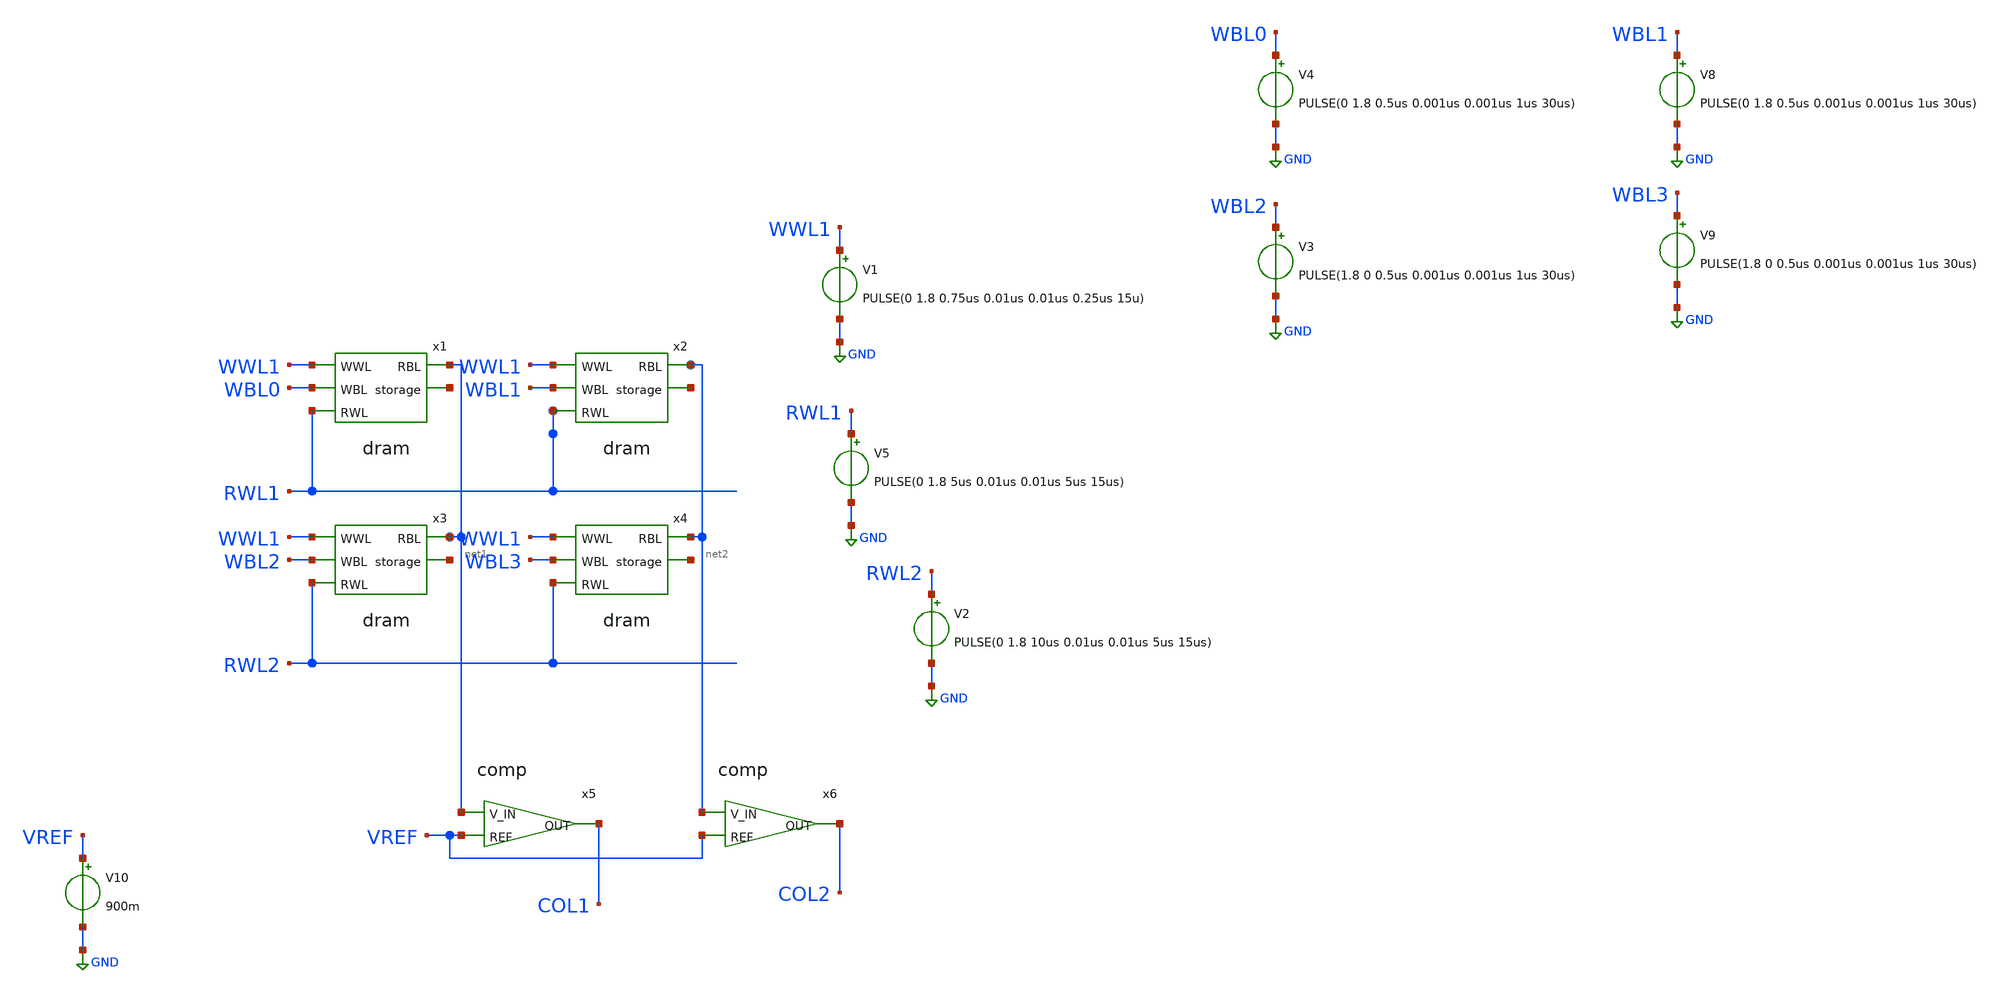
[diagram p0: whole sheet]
** sch_path: xschem/digital_prims/dram_tb.sch
**.subckt dram_tb
V1 WWL1 GND PULSE(0 1.8 0.75us 0.01us 0.01us 0.25us 15u)
V4 WBL0 GND PULSE(0 1.8 0.5us 0.001us 0.001us 1us 30us)
V5 RWL1 GND PULSE(0 1.8 5us 0.01us 0.01us 5us 15us)
x1 WWL1 net1 net3 WBL0 RWL1 dram
x2 WWL1 net2 net4 WBL1 RWL1 dram
x3 WWL1 net1 net5 WBL2 RWL2 dram
x4 WWL1 net2 net6 WBL3 RWL2 dram
V2 RWL2 GND PULSE(0 1.8 10us 0.01us 0.01us 5us 15us)
V3 WBL2 GND PULSE(1.8 0 0.5us 0.001us 0.001us 1us 30us)
V8 WBL1 GND PULSE(0 1.8 0.5us 0.001us 0.001us 1us 30us)
V9 WBL3 GND PULSE(1.8 0 0.5us 0.001us 0.001us 1us 30us)
x5 COL1 net1 VREF comp
x6 COL2 net2 VREF comp
V10 VREF GND 900m
**** begin user architecture code

** opencircuitdesign pdks install
.lib $::SKYWATER_MODELS/sky130.lib.spice tt


**** end user architecture code
**.ends

* expanding   symbol:  dram.sym # of pins=5
** sym_path: xschem/digital_prims/dram.sym
** sch_path: xschem/digital_prims/dram.sch
.subckt dram WWL RBL storage WBL RWL
*.opin RBL
*.ipin RWL
*.ipin WBL
*.ipin WWL
*.opin storage
XM3 RWL storage RBL GND sky130_fd_pr__nfet_01v8 L=0.15 W=1 nf=1 ad='int((nf+1)/2) * W/nf * 0.29' as='int((nf+2)/2) * W/nf * 0.29'
+ pd='2*int((nf+1)/2) * (W/nf + 0.29)' ps='2*int((nf+2)/2) * (W/nf + 0.29)' nrd='0.29 / W' nrs='0.29 / W'
+ sa=0 sb=0 sd=0 mult=1 m=1
XM1 WBL WWL storage GND sky130_fd_pr__nfet_01v8 L=0.15 W=1 nf=1 ad='int((nf+1)/2) * W/nf * 0.29' as='int((nf+2)/2) * W/nf * 0.29'
+ pd='2*int((nf+1)/2) * (W/nf + 0.29)' ps='2*int((nf+2)/2) * (W/nf + 0.29)' nrd='0.29 / W' nrs='0.29 / W'
+ sa=0 sb=0 sd=0 mult=1 m=1
.ends


* expanding   symbol:  comp.sym # of pins=3
** sym_path: xschem/comp.sym
** sch_path: xschem/comp.sch
.subckt comp OUT V_IN REF
*.ipin REF
*.ipin V_IN
*.opin OUT
XM5 net1 GN VCC VCC sky130_fd_pr__pfet_01v8_lvt L=1 W=1 nf=1 ad='W * 0.29' as='W * 0.29' pd='2*(W + 0.29)'
+ ps='2*(W + 0.29)' nrd=0 nrs=0 sa=0 sb=0 sd=0 mult=1 m=1
XM6 GN GN VCC VCC sky130_fd_pr__pfet_01v8_lvt L=1 W=1 nf=1 ad='W * 0.29' as='W * 0.29' pd='2*(W + 0.29)'
+ ps='2*(W + 0.29)' nrd=0 nrs=0 sa=0 sb=0 sd=0 mult=1 m=1
XM23 net1 V_IN SN GND sky130_fd_pr__nfet_01v8_lvt L=0.15 W=1 nf=1 ad='W * 0.29' as='W * 0.29' pd='2*(W + 0.29)'
+ ps='2*(W + 0.29)' nrd=0 nrs=0 sa=0 sb=0 sd=0 mult=1 m=1
XM16 GN REF SN GND sky130_fd_pr__nfet_01v8_lvt L=0.15 W=1 nf=1 ad='W * 0.29' as='W * 0.29' pd='2*(W + 0.29)'
+ ps='2*(W + 0.29)' nrd=0 nrs=0 sa=0 sb=0 sd=0 mult=1 m=1
I0 SN GND 100n
XM1 OUT net1 GND GND sky130_fd_pr__nfet_01v8_lvt L=0.15 W=1 nf=1 ad='W * 0.29' as='W * 0.29' pd='2*(W + 0.29)'
+ ps='2*(W + 0.29)' nrd=0 nrs=0 sa=0 sb=0 sd=0 mult=1 m=1
XM2 OUT net1 VCC VCC sky130_fd_pr__pfet_01v8_lvt L=0.35 W=2 nf=1 ad='W * 0.29' as='W * 0.29' pd='2*(W + 0.29)'
+ ps='2*(W + 0.29)' nrd=0 nrs=0 sa=0 sb=0 sd=0 mult=1 m=1
V1 VCC GND 1.8
.ends

.GLOBAL GND
**** begin user architecture code


.control
save all

tran 0.1us 200us
plot v(BL)
.endc


**** end user architecture code
.end
